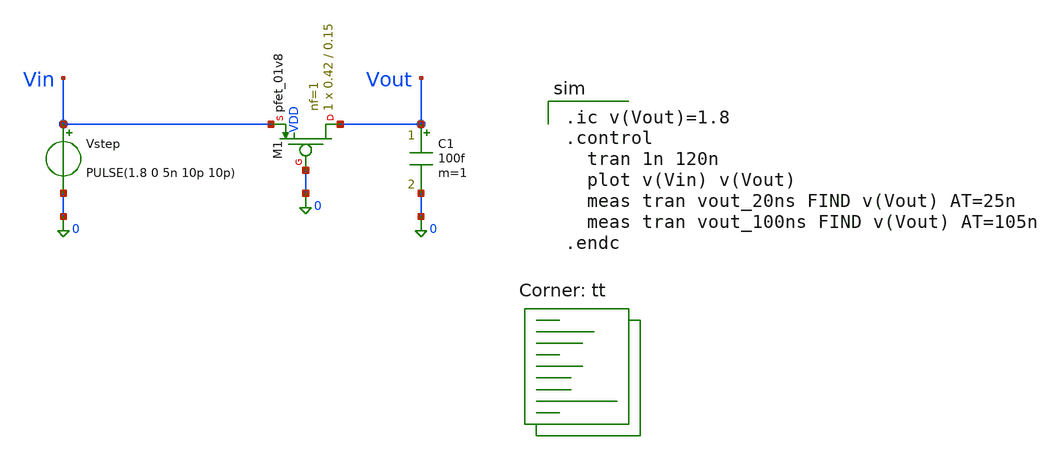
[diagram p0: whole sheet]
** sch_path: tutorial-1/source/q3d.sch
**.subckt q3d
C1 Vout 0 100f m=1
Vstep Vin 0 PULSE(1.8 0 5n 10p 10p)
XM1 Vout 0 Vin VDD sky130_fd_pr__pfet_01v8 L=0.15 W=0.42 nf=1 ad='int((nf+1)/2) * W/nf * 0.29' as='int((nf+2)/2) * W/nf * 0.29'
+ pd='2*int((nf+1)/2) * (W/nf + 0.29)' ps='2*int((nf+2)/2) * (W/nf + 0.29)' nrd='0.29 / W' nrs='0.29 / W'
+ sa=0 sb=0 sd=0 mult=1 m=1
**** begin user architecture code

.ic v(Vout)=1.8
.control
  tran 1n 120n
  plot v(Vin) v(Vout)
  meas tran vout_20ns FIND v(Vout) AT=25n
  meas tran vout_100ns FIND v(Vout) AT=105n
.endc

.lib $::SKYWATER_MODELS/sky130.lib.spice tt
**** end user architecture code
**.ends
.end
